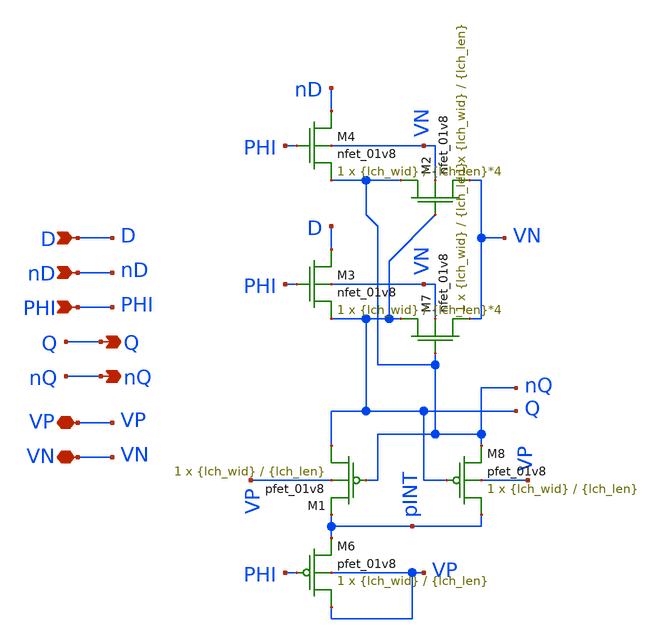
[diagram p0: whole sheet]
** sch_path: csrl_latch2.sch
**.subckt csrl_latch2 VP D Q nD PHI nQ VN
*.iopin VP
*.ipin D
*.opin Q
*.ipin nD
*.ipin PHI
*.opin nQ
*.iopin VN
XM8 pINT Q nQ VP sky130_fd_pr__pfet_01v8 L={lch_len} W={lch_wid} nf=1 ad='int((nf+1)/2) * W/nf * 0.29'
+ as='int((nf+2)/2) * W/nf * 0.29' pd='2*int((nf+1)/2) * (W/nf + 0.29)' ps='2*int((nf+2)/2) * (W/nf + 0.29)'
+ nrd='0.29 / W' nrs='0.29 / W' sa=0 sb=0 sd=0 mult=1 m=1
XM1 Q nQ pINT VP sky130_fd_pr__pfet_01v8 L={lch_len} W={lch_wid} nf=1 ad='int((nf+1)/2) * W/nf * 0.29'
+ as='int((nf+2)/2) * W/nf * 0.29' pd='2*int((nf+1)/2) * (W/nf + 0.29)' ps='2*int((nf+2)/2) * (W/nf + 0.29)'
+ nrd='0.29 / W' nrs='0.29 / W' sa=0 sb=0 sd=0 mult=1 m=1
XM6 VP PHI pINT VP sky130_fd_pr__pfet_01v8 L={lch_len} W={lch_wid} nf=1 ad='int((nf+1)/2) * W/nf * 0.29'
+ as='int((nf+2)/2) * W/nf * 0.29' pd='2*int((nf+1)/2) * (W/nf + 0.29)' ps='2*int((nf+2)/2) * (W/nf + 0.29)'
+ nrd='0.29 / W' nrs='0.29 / W' sa=0 sb=0 sd=0 mult=1 m=1
XM7 Q nQ VN VN sky130_fd_pr__nfet_01v8 L={lch_len} W={lch_wid} nf=1 ad='int((nf+1)/2) * W/nf * 0.29'
+ as='int((nf+2)/2) * W/nf * 0.29' pd='2*int((nf+1)/2) * (W/nf + 0.29)' ps='2*int((nf+2)/2) * (W/nf + 0.29)'
+ nrd='0.29 / W' nrs='0.29 / W' sa=0 sb=0 sd=0 mult=1 m=1
XM2 nQ Q VN VN sky130_fd_pr__nfet_01v8 L={lch_len} W={lch_wid} nf=1 ad='int((nf+1)/2) * W/nf * 0.29'
+ as='int((nf+2)/2) * W/nf * 0.29' pd='2*int((nf+1)/2) * (W/nf + 0.29)' ps='2*int((nf+2)/2) * (W/nf + 0.29)'
+ nrd='0.29 / W' nrs='0.29 / W' sa=0 sb=0 sd=0 mult=1 m=1
XM3 D PHI Q VN sky130_fd_pr__nfet_01v8 L={lch_len}*4 W={lch_wid} nf=1 ad='int((nf+1)/2) * W/nf * 0.29'
+ as='int((nf+2)/2) * W/nf * 0.29' pd='2*int((nf+1)/2) * (W/nf + 0.29)' ps='2*int((nf+2)/2) * (W/nf + 0.29)'
+ nrd='0.29 / W' nrs='0.29 / W' sa=0 sb=0 sd=0 mult=1 m=1
XM4 nD PHI nQ VN sky130_fd_pr__nfet_01v8 L={lch_len}*4 W={lch_wid} nf=1 ad='int((nf+1)/2) * W/nf * 0.29'
+ as='int((nf+2)/2) * W/nf * 0.29' pd='2*int((nf+1)/2) * (W/nf + 0.29)' ps='2*int((nf+2)/2) * (W/nf + 0.29)'
+ nrd='0.29 / W' nrs='0.29 / W' sa=0 sb=0 sd=0 mult=1 m=1
**.ends
.end
